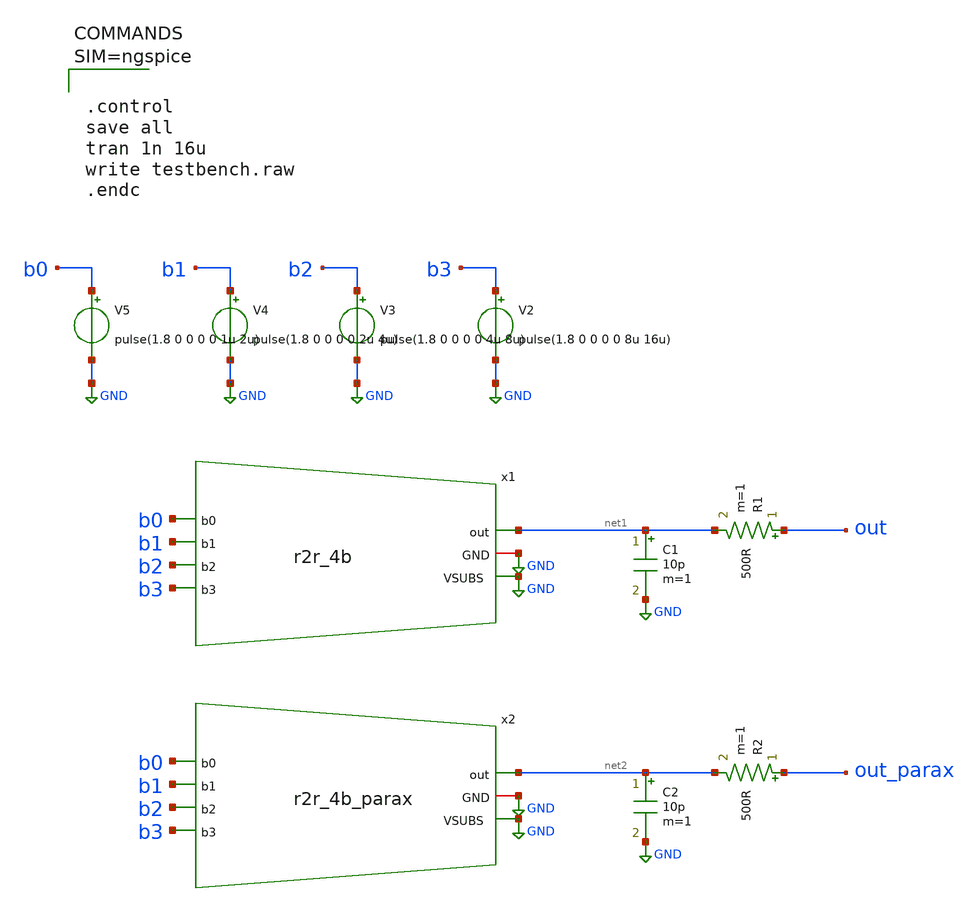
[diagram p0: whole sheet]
** sch_path: xschem/testbench.sch
**.subckt testbench
x1 net1 GND GND b3 b1 b2 b0 r2r_4b
R1 out net1 500R m=1
C1 net1 GND 10p m=1
V2 b3 GND pulse(1.8 0 0 0 0 8u 16u)
V3 b2 GND pulse(1.8 0 0 0 0 4u 8u)
V4 b1 GND pulse(1.8 0 0 0 0 2u 4u)
V5 b0 GND pulse(1.8 0 0 0 0 1u 2u)
x2 net2 GND GND b3 b1 b2 b0 r2r_4b_parax
R2 out_parax net2 500R m=1
C2 net2 GND 10p m=1
**** begin user architecture code

** opencircuitdesign pdks install
.lib $::SKYWATER_MODELS/sky130.lib.spice tt
.include $::SKYWATER_STDCELLS/sky130_fd_sc_hd.spice




.control
save all
tran 1n 16u
write testbench.raw
.endc



**** end user architecture code
**.ends

* expanding   symbol:  r2r_4b.sym # of pins=7
** sym_path: xschem/r2r_4b.sym
** sch_path: xschem/r2r_4b.sch
.subckt r2r_4b out GND VSUBS b3 b1 b2 b0
*.iopin GND
*.opin out
*.ipin b0
*.ipin b2
*.ipin b1
*.ipin b3
*.ipin VSUBS
XR2 net1 GND VSUBS sky130_fd_pr__res_high_po_0p35 L=40 mult=1 m=1
XR9 net2 net1 VSUBS sky130_fd_pr__res_high_po_0p35 L=20 mult=1 m=1
XR1 net1 b0 VSUBS sky130_fd_pr__res_high_po_0p35 L=40 mult=1 m=1
XR3 net3 net2 VSUBS sky130_fd_pr__res_high_po_0p35 L=20 mult=1 m=1
XR4 net2 b1 VSUBS sky130_fd_pr__res_high_po_0p35 L=40 mult=1 m=1
XR5 out net3 VSUBS sky130_fd_pr__res_high_po_0p35 L=20 mult=1 m=1
XR6 net3 b2 VSUBS sky130_fd_pr__res_high_po_0p35 L=40 mult=1 m=1
XR7 out b3 VSUBS sky130_fd_pr__res_high_po_0p35 L=40 mult=1 m=1
.ends


* expanding   symbol:  r2r_4b_parax.sym # of pins=7
** sym_path: xschem/r2r_4b.sym
.include [file normalize ../mag/r2r_4b.sim.spice]
.GLOBAL GND
.end
